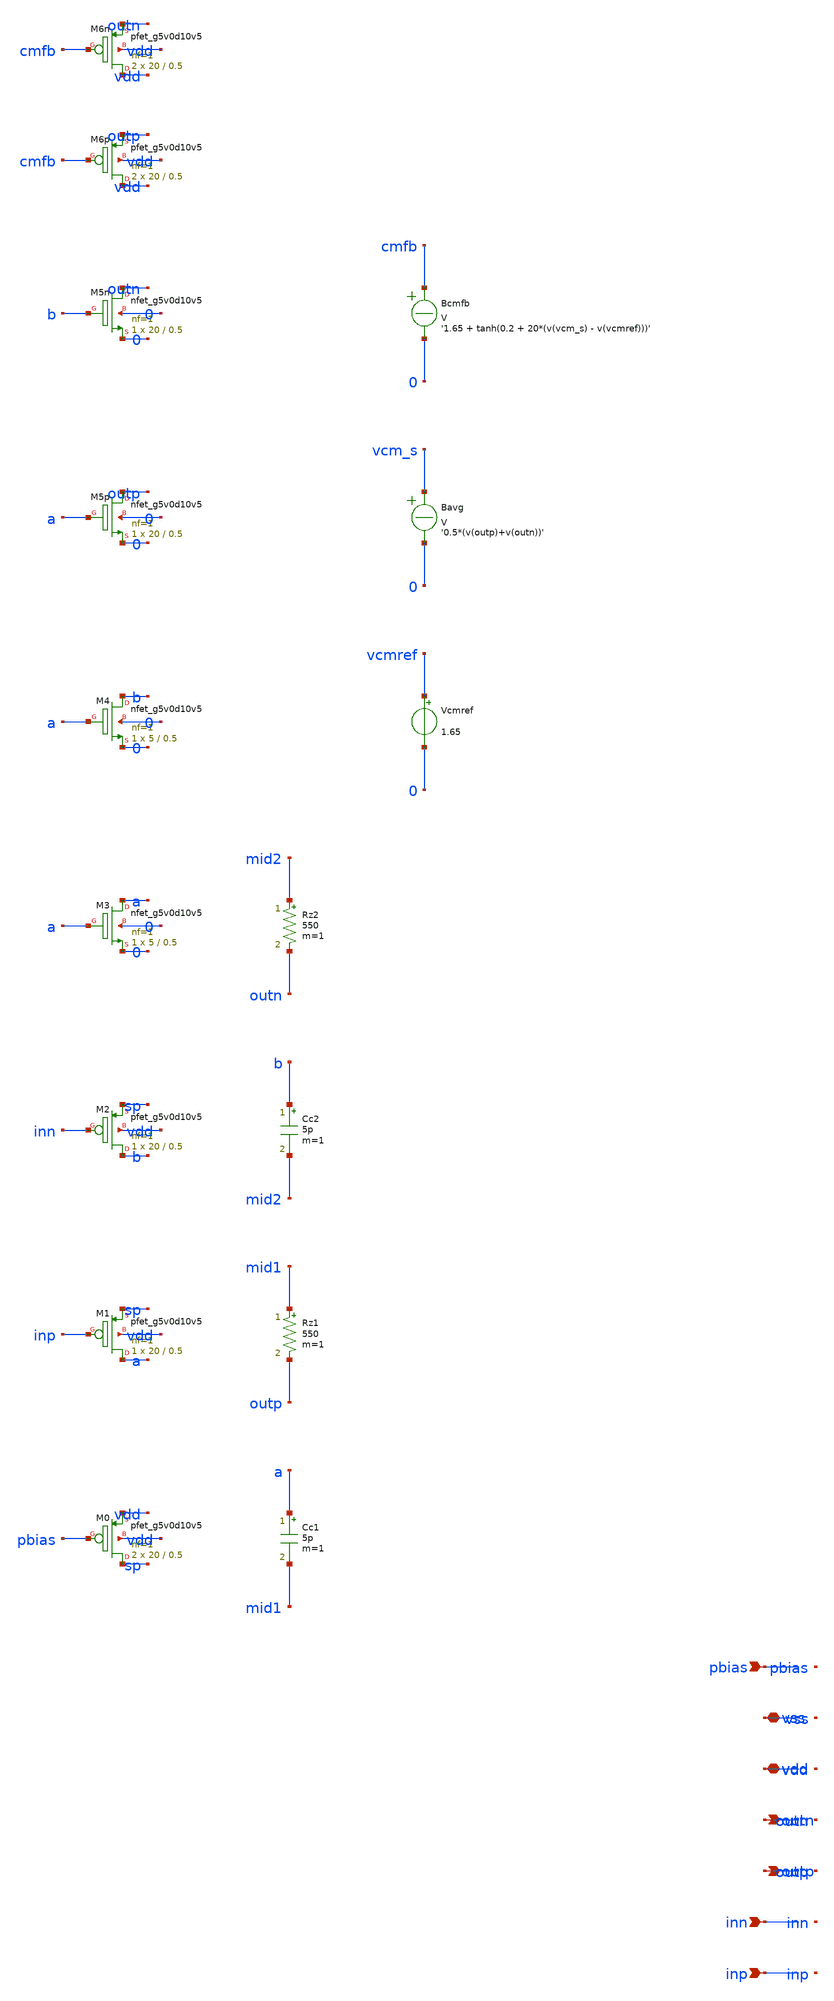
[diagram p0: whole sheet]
** sch_path: design/opamp/opamp_2stage.sch
* SPDX-License-Identifier: Apache-2.0
**.subckt opamp_2stage inp inn outp outn vdd vss pbias
*.ipin inp
*.ipin inn
*.opin outp
*.opin outn
*.iopin vdd
*.iopin vss
*.ipin pbias
XM0 sp pbias vdd vdd sky130_fd_pr__pfet_g5v0d10v5 L=0.5 W=20 nf=1 ad='int((1 + 1)/2) * 20 / 1 * 0.29'
+ as='int((1 + 2)/2) * 20 / 1 * 0.29' pd='2*int((1 + 1)/2) * (20 / 1 + 0.29)' ps='2*int((1 + 2)/2) * (20 / 1 + 0.29)'
+ nrd='0.29 / 20 ' nrs='0.29 / 20 ' sa=0 sb=0 sd=0 mult=2 m=2
XM1 a inp sp vdd sky130_fd_pr__pfet_g5v0d10v5 L=0.5 W=20 nf=1 ad='int((1 + 1)/2) * 20 / 1 * 0.29' as='int((1 + 2)/2) * 20 / 1 * 0.29'
+ pd='2*int((1 + 1)/2) * (20 / 1 + 0.29)' ps='2*int((1 + 2)/2) * (20 / 1 + 0.29)' nrd='0.29 / 20 ' nrs='0.29 / 20 '
+ sa=0 sb=0 sd=0 mult=1 m=1
XM2 b inn sp vdd sky130_fd_pr__pfet_g5v0d10v5 L=0.5 W=20 nf=1 ad='int((1 + 1)/2) * 20 / 1 * 0.29' as='int((1 + 2)/2) * 20 / 1 * 0.29'
+ pd='2*int((1 + 1)/2) * (20 / 1 + 0.29)' ps='2*int((1 + 2)/2) * (20 / 1 + 0.29)' nrd='0.29 / 20 ' nrs='0.29 / 20 '
+ sa=0 sb=0 sd=0 mult=1 m=1
XM3 a a 0 0 sky130_fd_pr__nfet_g5v0d10v5 L=0.5 W=5 nf=1 ad='int((1 + 1)/2) * 5 / 1 * 0.29' as='int((1 + 2)/2) * 5 / 1 * 0.29'
+ pd='2*int((1 + 1)/2) * (5 / 1 + 0.29)' ps='2*int((1 + 2)/2) * (5 / 1 + 0.29)' nrd='0.29 / 5 ' nrs='0.29 / 5 '
+ sa=0 sb=0 sd=0 mult=1 m=1
XM4 b a 0 0 sky130_fd_pr__nfet_g5v0d10v5 L=0.5 W=5 nf=1 ad='int((1 + 1)/2) * 5 / 1 * 0.29' as='int((1 + 2)/2) * 5 / 1 * 0.29'
+ pd='2*int((1 + 1)/2) * (5 / 1 + 0.29)' ps='2*int((1 + 2)/2) * (5 / 1 + 0.29)' nrd='0.29 / 5 ' nrs='0.29 / 5 '
+ sa=0 sb=0 sd=0 mult=1 m=1
XM5p outp a 0 0 sky130_fd_pr__nfet_g5v0d10v5 L=0.5 W=20 nf=1 ad='int((1 + 1)/2) * 20 / 1 * 0.29' as='int((1 + 2)/2) * 20 / 1 * 0.29'
+ pd='2*int((1 + 1)/2) * (20 / 1 + 0.29)' ps='2*int((1 + 2)/2) * (20 / 1 + 0.29)' nrd='0.29 / 20 ' nrs='0.29 / 20 '
+ sa=0 sb=0 sd=0 mult=1 m=1
XM5n outn b 0 0 sky130_fd_pr__nfet_g5v0d10v5 L=0.5 W=20 nf=1 ad='int((1 + 1)/2) * 20 / 1 * 0.29' as='int((1 + 2)/2) * 20 / 1 * 0.29'
+ pd='2*int((1 + 1)/2) * (20 / 1 + 0.29)' ps='2*int((1 + 2)/2) * (20 / 1 + 0.29)' nrd='0.29 / 20 ' nrs='0.29 / 20 '
+ sa=0 sb=0 sd=0 mult=1 m=1
XM6p vdd cmfb outp vdd sky130_fd_pr__pfet_g5v0d10v5 L=0.5 W=20 nf=1 ad='int((1 + 1)/2) * 20 / 1 * 0.29'
+ as='int((1 + 2)/2) * 20 / 1 * 0.29' pd='2*int((1 + 1)/2) * (20 / 1 + 0.29)' ps='2*int((1 + 2)/2) * (20 / 1 + 0.29)'
+ nrd='0.29 / 20 ' nrs='0.29 / 20 ' sa=0 sb=0 sd=0 mult=2 m=2
XM6n vdd cmfb outn vdd sky130_fd_pr__pfet_g5v0d10v5 L=0.5 W=20 nf=1 ad='int((1 + 1)/2) * 20 / 1 * 0.29'
+ as='int((1 + 2)/2) * 20 / 1 * 0.29' pd='2*int((1 + 1)/2) * (20 / 1 + 0.29)' ps='2*int((1 + 2)/2) * (20 / 1 + 0.29)'
+ nrd='0.29 / 20 ' nrs='0.29 / 20 ' sa=0 sb=0 sd=0 mult=2 m=2
Cc1 a mid1 5p m=1
Rz1 mid1 outp 550 m=1
Cc2 b mid2 5p m=1
Rz2 mid2 outn 550 m=1
Vcmref vcmref 0 1.65
Bavg vcm_s 0 V = '0.5*(v(outp)+v(outn))' m=1
Bcmfb cmfb 0 V = '1.65 + tanh(0.2 + 20*(v(vcm_s) - v(vcmref)))' m=1
**.ends
.end
